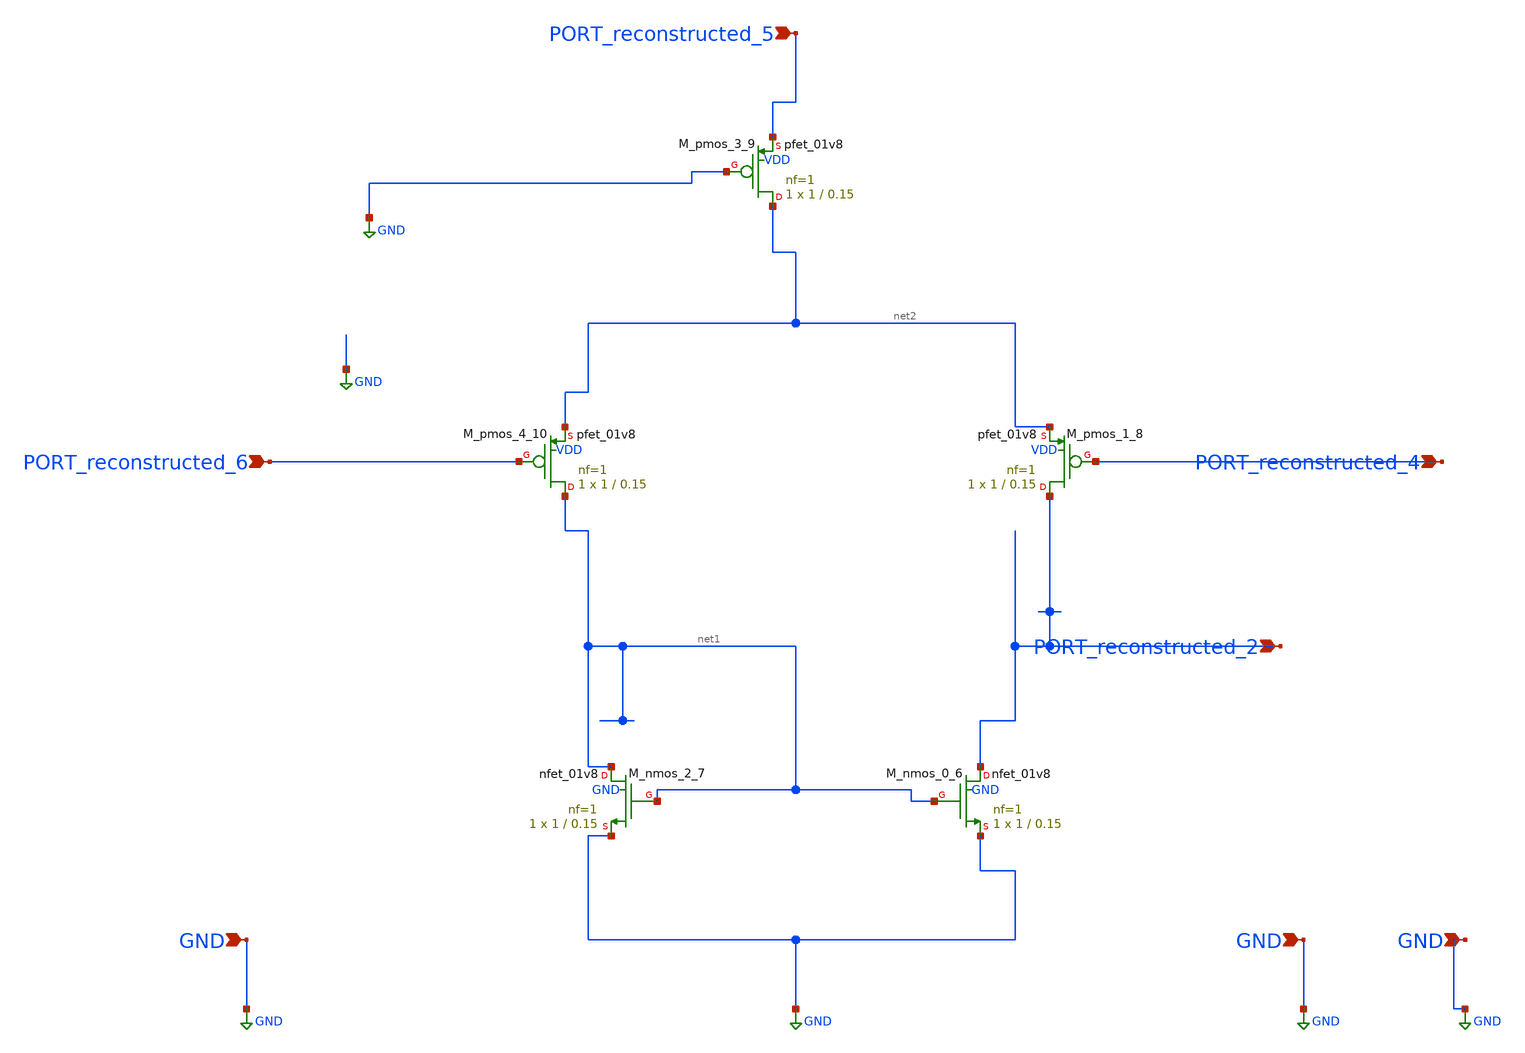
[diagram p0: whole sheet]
** sch_path: schematics/Image2Net/015.sch
**.subckt 015 GND PORT_reconstructed_2 PORT_reconstructed_6 GND GND PORT_reconstructed_5
*+ PORT_reconstructed_4
*.ipin GND
*.ipin PORT_reconstructed_2
*.ipin PORT_reconstructed_6
*.ipin GND
*.ipin GND
*.ipin PORT_reconstructed_5
*.ipin PORT_reconstructed_4
XM_nmos_0_6 PORT_reconstructed_2 net1 GND GND sky130_fd_pr__nfet_01v8 L=0.15 W=1 nf=1 ad='int((1 + 1)/2) * 1 / 1 * 0.29'
+ as='int((1 + 2)/2) * 1 / 1 * 0.29' pd='2*int((1 + 1)/2) * (1 / 1 + 0.29)' ps='2*int((1 + 2)/2) * (1 / 1 + 0.29)'
+ nrd='0.29 / 1 ' nrs='0.29 / 1 ' sa=0 sb=0 sd=0 mult=1 m=1
XM_nmos_2_7 net1 net1 GND GND sky130_fd_pr__nfet_01v8 L=0.15 W=1 nf=1 ad='int((1 + 1)/2) * 1 / 1 * 0.29'
+ as='int((1 + 2)/2) * 1 / 1 * 0.29' pd='2*int((1 + 1)/2) * (1 / 1 + 0.29)' ps='2*int((1 + 2)/2) * (1 / 1 + 0.29)'
+ nrd='0.29 / 1 ' nrs='0.29 / 1 ' sa=0 sb=0 sd=0 mult=1 m=1
XM_pmos_1_8 PORT_reconstructed_2 PORT_reconstructed_4 net2 VDD sky130_fd_pr__pfet_01v8 L=0.15 W=1 nf=1
+ ad='int((1 + 1)/2) * 1 / 1 * 0.29' as='int((1 + 2)/2) * 1 / 1 * 0.29' pd='2*int((1 + 1)/2) * (1 / 1 + 0.29)'
+ ps='2*int((1 + 2)/2) * (1 / 1 + 0.29)' nrd='0.29 / 1 ' nrs='0.29 / 1 ' sa=0 sb=0 sd=0 mult=1 m=1
XM_pmos_3_9 net2 GND PORT_reconstructed_5 VDD sky130_fd_pr__pfet_01v8 L=0.15 W=1 nf=1 ad='int((1 + 1)/2) * 1 / 1 * 0.29'
+ as='int((1 + 2)/2) * 1 / 1 * 0.29' pd='2*int((1 + 1)/2) * (1 / 1 + 0.29)' ps='2*int((1 + 2)/2) * (1 / 1 + 0.29)'
+ nrd='0.29 / 1 ' nrs='0.29 / 1 ' sa=0 sb=0 sd=0 mult=1 m=1
XM_pmos_4_10 net1 PORT_reconstructed_6 net2 VDD sky130_fd_pr__pfet_01v8 L=0.15 W=1 nf=1 ad='int((1 + 1)/2) * 1 / 1 * 0.29'
+ as='int((1 + 2)/2) * 1 / 1 * 0.29' pd='2*int((1 + 1)/2) * (1 / 1 + 0.29)' ps='2*int((1 + 2)/2) * (1 / 1 + 0.29)'
+ nrd='0.29 / 1 ' nrs='0.29 / 1 ' sa=0 sb=0 sd=0 mult=1 m=1
**.ends
.GLOBAL GND
.end
